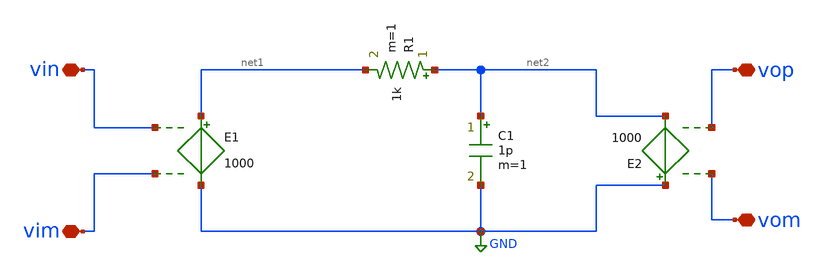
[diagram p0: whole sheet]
** sch_path: xschem/untitled-4.sch
**.subckt untitled-4 vim vin vom vop
*.iopin vim
*.iopin vin
*.iopin vom
*.iopin vop
E1 net1 GND vin vim 1000
E2 GND net2 vom vop 1000
R1 net2 net1 1k m=1
C1 net2 GND 1p m=1
**.ends
.GLOBAL GND
.end
